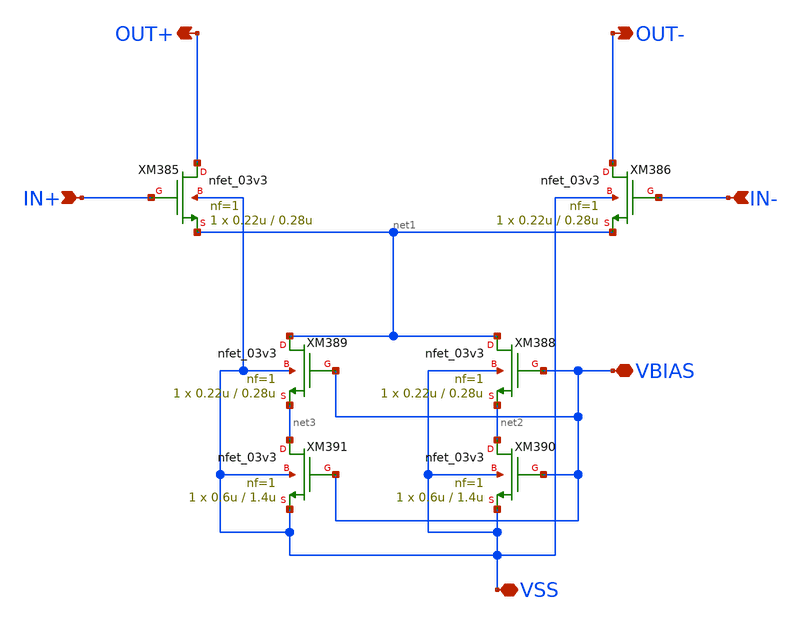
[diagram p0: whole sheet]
** sch_path: xschem/CS_Switch_4x.sch
**.subckt CS_Switch_4x IN+ IN- OUT+ OUT- VBIAS VSS
*.ipin IN+
*.ipin IN-
*.opin OUT+
*.opin OUT-
*.iopin VBIAS
*.iopin VSS
XM385 OUT+ IN+ net1 VSS nfet_03v3 L=0.28u W=0.22u nf=1 ad='int((nf+1)/2) * W/nf * 0.18u' as='int((nf+2)/2) * W/nf * 0.18u'
+ pd='2*int((nf+1)/2) * (W/nf + 0.18u)' ps='2*int((nf+2)/2) * (W/nf + 0.18u)' nrd='0.18u / W' nrs='0.18u / W'
+ sa=0 sb=0 sd=0 m=1
XM386 OUT- IN- net1 VSS nfet_03v3 L=0.28u W=0.22u nf=1 ad='int((nf+1)/2) * W/nf * 0.18u' as='int((nf+2)/2) * W/nf * 0.18u'
+ pd='2*int((nf+1)/2) * (W/nf + 0.18u)' ps='2*int((nf+2)/2) * (W/nf + 0.18u)' nrd='0.18u / W' nrs='0.18u / W'
+ sa=0 sb=0 sd=0 m=1
XM388 net1 VBIAS net2 VSS nfet_03v3 L=0.28u W=0.22u nf=1 ad='int((nf+1)/2) * W/nf * 0.18u' as='int((nf+2)/2) * W/nf * 0.18u'
+ pd='2*int((nf+1)/2) * (W/nf + 0.18u)' ps='2*int((nf+2)/2) * (W/nf + 0.18u)' nrd='0.18u / W' nrs='0.18u / W'
+ sa=0 sb=0 sd=0 m=1
XM389 net1 VBIAS net3 VSS nfet_03v3 L=0.28u W=0.22u nf=1 ad='int((nf+1)/2) * W/nf * 0.18u' as='int((nf+2)/2) * W/nf * 0.18u'
+ pd='2*int((nf+1)/2) * (W/nf + 0.18u)' ps='2*int((nf+2)/2) * (W/nf + 0.18u)' nrd='0.18u / W' nrs='0.18u / W'
+ sa=0 sb=0 sd=0 m=1
XM390 net2 VBIAS VSS VSS nfet_03v3 L=1.4u W=0.6u nf=1 ad='int((nf+1)/2) * W/nf * 0.18u' as='int((nf+2)/2) * W/nf * 0.18u'
+ pd='2*int((nf+1)/2) * (W/nf + 0.18u)' ps='2*int((nf+2)/2) * (W/nf + 0.18u)' nrd='0.18u / W' nrs='0.18u / W'
+ sa=0 sb=0 sd=0 m=1
XM391 net3 VBIAS VSS VSS nfet_03v3 L=1.4u W=0.6u nf=1 ad='int((nf+1)/2) * W/nf * 0.18u' as='int((nf+2)/2) * W/nf * 0.18u'
+ pd='2*int((nf+1)/2) * (W/nf + 0.18u)' ps='2*int((nf+2)/2) * (W/nf + 0.18u)' nrd='0.18u / W' nrs='0.18u / W'
+ sa=0 sb=0 sd=0 m=1
**.ends
.end
